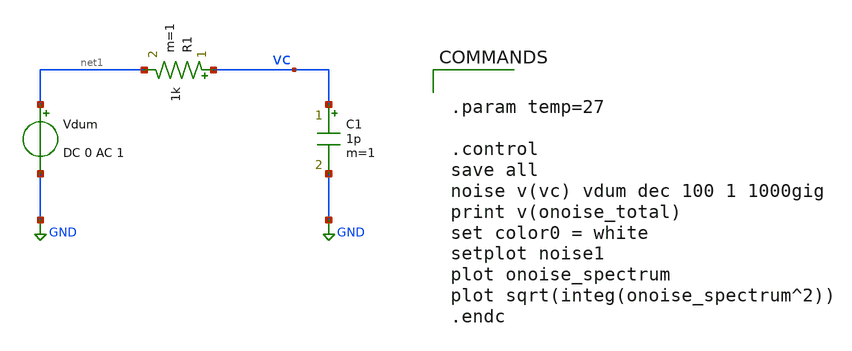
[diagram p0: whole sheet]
** sch_path: 5_Design/3_Real_circuits/sandbox_boris/tb_res_noise.sch
**.subckt tb_res_noise
R1 vc net1 1k m=1
C1 vc GND 1p m=1
Vdum net1 GND DC 0 AC 1
**** begin user architecture code


.param temp=27

.control
save all
noise v(vc) vdum dec 100 1 1000gig
print v(onoise_total)
set color0 = white
setplot noise1
plot onoise_spectrum
plot sqrt(integ(onoise_spectrum^2))
.endc


**** end user architecture code
**.ends
.GLOBAL GND
.end
